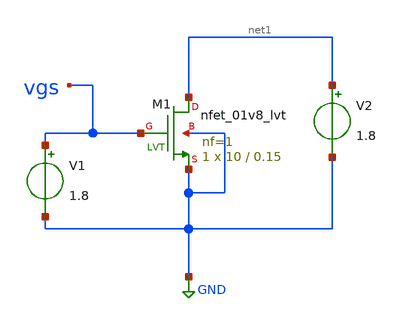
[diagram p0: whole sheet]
** sch_path: circuits-pub/LNA/LNA-spice.sch
**.subckt LNA-spice
XM1 net1 vgs GND GND sky130_fd_pr__nfet_01v8_lvt L=0.15 W=10 nf=1 ad='int((nf+1)/2) * W/nf * 0.29' as='int((nf+2)/2) * W/nf * 0.29'
+ pd='2*int((nf+1)/2) * (W/nf + 0.29)' ps='2*int((nf+2)/2) * (W/nf + 0.29)' nrd='0.29 / W' nrs='0.29 / W'
+ sa=0 sb=0 sd=0 mult=1 m=1
V1 vgs GND 1.8
V2 net1 GND 1.8
**** begin user architecture code


.include init.txt

.control
save all

save @m.xm1.msky130_fd_pr__nfet_01v8_lvt[id]
save @m.xm1.msky130_fd_pr__nfet_01v8_lvt[gm]
save @m.xm1.msky130_fd_pr__nfet_01v8_lvt[cgg]

dc V1 0 1.8 1m

let id=@m.xm1.msky130_fd_pr__nfet_01v8_lvt[id]
let gm=@m.xm1.msky130_fd_pr__nfet_01v8_lvt[gm]
let cgg=@m.xm1.msky130_fd_pr__nfet_01v8_lvt[cgg]

let ft = gm/(2*pi*cgg)




.endc









**** end user architecture code
**.ends
.GLOBAL GND
.end
